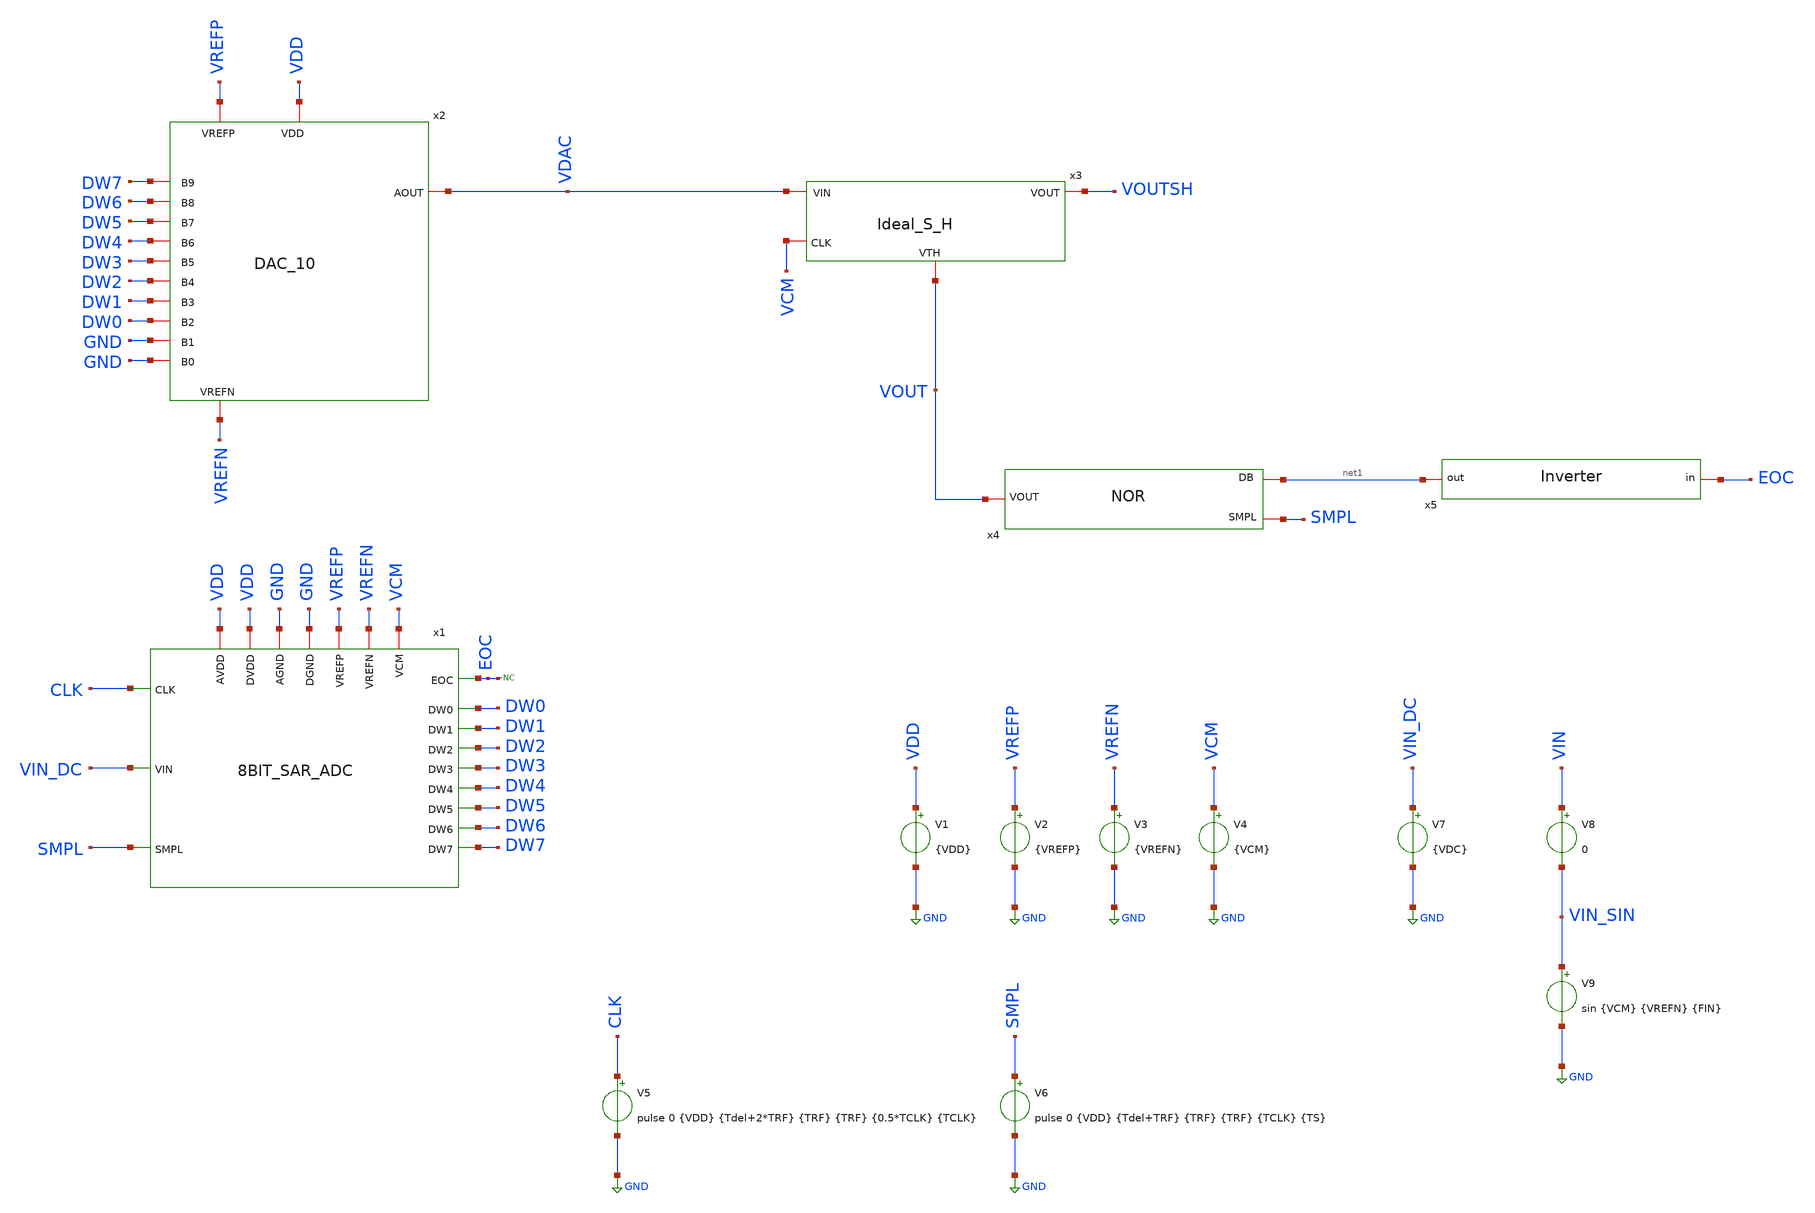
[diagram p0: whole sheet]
** sch_path: Designs/SAR_tb.sch
**.subckt SAR_tb
x2 VREFP VDD VDAC DW3 DW2 DW6 GND DW4 GND DW0 DW1 DW5 DW7 VREFN DAC_10
x3 VCM VOUT VOUTSH VDAC Ideal_S_H
x4 SMPL VOUT net1 NOR TRF=100p
x5 EOC net1 INV TRF=100p
V1 VDD GND {VDD}
V2 VREFP GND {VREFP}
V3 VREFN GND {VREFN}
V4 VCM GND {VCM}
V5 CLK GND pulse 0 {VDD} {Tdel+2*TRF} {TRF} {TRF} {0.5*TCLK} {TCLK}
V6 SMPL GND pulse 0 {VDD} {Tdel+TRF} {TRF} {TRF} {TCLK} {TS}
V7 VIN_DC GND {VDC}
V8 VIN VIN_SIN 0
V9 VIN_SIN GND sin {VCM} {VREFN} {FIN}
* noconn EOC
x1 VDD VIN_DC DW0 DW4 VREFP GND DW5 DW1 CLK VREFN VCM DW2 SMPL VDD DW6 DW3 DW7 GND EOC 8BIT_SAR_ADC
**** begin user architecture code


.param vcc=VDD
*.options filetype=ascii
.param CU=20f CP=5p
.param Tdel=50n TRF=100p TCLK=100n NBIT=8 TS=1u
.param VDD =2 VREFP=0.75*VDD VREFN=0.25*VDD VCM=(VREFP+VREFN)/2
.param VDC=0.7
****DC_simulation****
.param TSTOP=4*TS TDROP=TS
****Sine_wave****
.param NFFT=2**7 NCYC=5 FIN=(NCYC/NFFT)/TS
*.param TSTOP=(NCYC/FIN)+TDROP TDROP=(0.5/FIN)+0.5*TS
.tran 50n {TSTOP} {TDROP}
.save v(VOUTSH) v(VDAC) v(VIN_DC) v(VOUT)
.save all

*options for an accurate precision output
.options reltol=1m vntol=1m abstol=1n




.include $::180MCU_MODELS/design.ngspice
.lib $::180MCU_MODELS/sm141064.ngspice typical
.model SWITCH1 sw vt=0

**** end user architecture code
**.ends
.GLOBAL GND
.end
